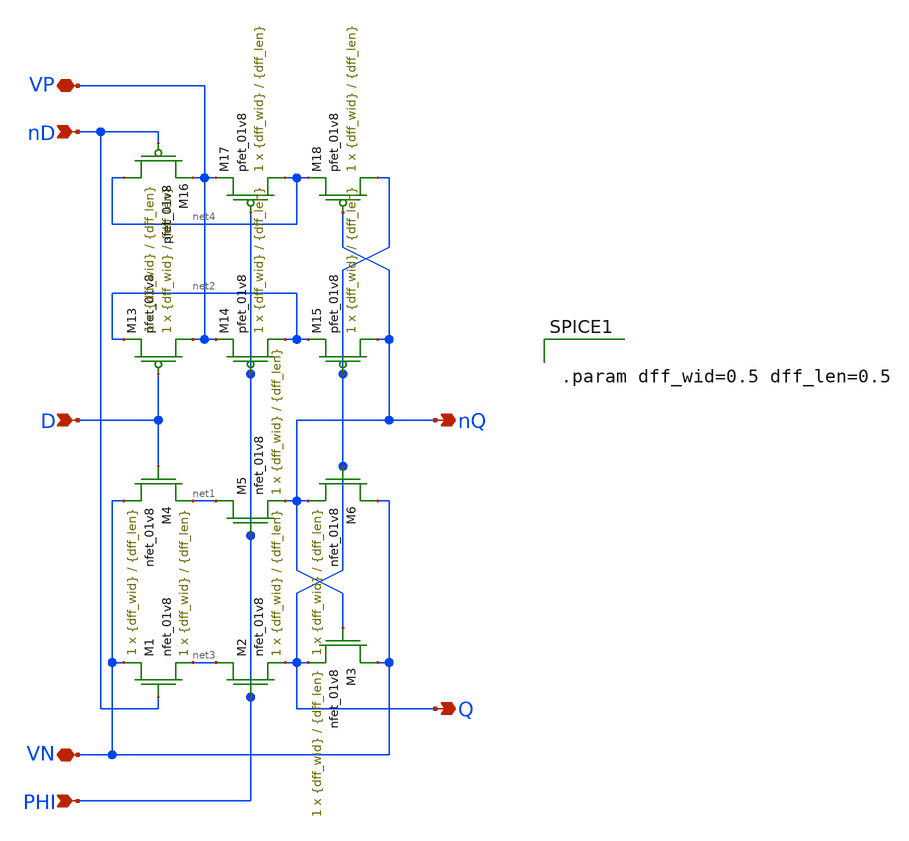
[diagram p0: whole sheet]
** sch_path: LDS/LDS_n_csrl_latch.sch
**.subckt LDS_n_csrl_latch D nD nQ Q PHI VP VN
*.ipin D
*.ipin nD
*.opin nQ
*.opin Q
*.ipin PHI
*.iopin VP
*.iopin VN
XM1 VN nD net3 VN sky130_fd_pr__nfet_01v8 L={dff_len} W={dff_wid} nf=1 ad='int((nf+1)/2) * W/nf * 0.29'
+ as='int((nf+2)/2) * W/nf * 0.29' pd='2*int((nf+1)/2) * (W/nf + 0.29)' ps='2*int((nf+2)/2) * (W/nf + 0.29)'
+ nrd='0.29 / W' nrs='0.29 / W' sa=0 sb=0 sd=0 mult=1 m=1
XM2 net3 PHI Q VN sky130_fd_pr__nfet_01v8 L={dff_len} W={dff_wid} nf=1 ad='int((nf+1)/2) * W/nf * 0.29'
+ as='int((nf+2)/2) * W/nf * 0.29' pd='2*int((nf+1)/2) * (W/nf + 0.29)' ps='2*int((nf+2)/2) * (W/nf + 0.29)'
+ nrd='0.29 / W' nrs='0.29 / W' sa=0 sb=0 sd=0 mult=1 m=1
XM3 VN nQ Q VN sky130_fd_pr__nfet_01v8 L={dff_len} W={dff_wid} nf=1 ad='int((nf+1)/2) * W/nf * 0.29'
+ as='int((nf+2)/2) * W/nf * 0.29' pd='2*int((nf+1)/2) * (W/nf + 0.29)' ps='2*int((nf+2)/2) * (W/nf + 0.29)'
+ nrd='0.29 / W' nrs='0.29 / W' sa=0 sb=0 sd=0 mult=1 m=1
XM4 net1 D VN VN sky130_fd_pr__nfet_01v8 L={dff_len} W={dff_wid} nf=1 ad='int((nf+1)/2) * W/nf * 0.29'
+ as='int((nf+2)/2) * W/nf * 0.29' pd='2*int((nf+1)/2) * (W/nf + 0.29)' ps='2*int((nf+2)/2) * (W/nf + 0.29)'
+ nrd='0.29 / W' nrs='0.29 / W' sa=0 sb=0 sd=0 mult=1 m=1
XM5 net1 PHI nQ VN sky130_fd_pr__nfet_01v8 L={dff_len} W={dff_wid} nf=1 ad='int((nf+1)/2) * W/nf * 0.29'
+ as='int((nf+2)/2) * W/nf * 0.29' pd='2*int((nf+1)/2) * (W/nf + 0.29)' ps='2*int((nf+2)/2) * (W/nf + 0.29)'
+ nrd='0.29 / W' nrs='0.29 / W' sa=0 sb=0 sd=0 mult=1 m=1
XM6 VN Q nQ VN sky130_fd_pr__nfet_01v8 L={dff_len} W={dff_wid} nf=1 ad='int((nf+1)/2) * W/nf * 0.29'
+ as='int((nf+2)/2) * W/nf * 0.29' pd='2*int((nf+1)/2) * (W/nf + 0.29)' ps='2*int((nf+2)/2) * (W/nf + 0.29)'
+ nrd='0.29 / W' nrs='0.29 / W' sa=0 sb=0 sd=0 mult=1 m=1
XM13 VP D net2 VP sky130_fd_pr__pfet_01v8 L={dff_len} W={dff_wid} nf=1 ad='int((nf+1)/2) * W/nf * 0.29'
+ as='int((nf+2)/2) * W/nf * 0.29' pd='2*int((nf+1)/2) * (W/nf + 0.29)' ps='2*int((nf+2)/2) * (W/nf + 0.29)'
+ nrd='0.29 / W' nrs='0.29 / W' sa=0 sb=0 sd=0 mult=1 m=1
XM14 net2 PHI VP VP sky130_fd_pr__pfet_01v8 L={dff_len} W={dff_wid} nf=1 ad='int((nf+1)/2) * W/nf * 0.29'
+ as='int((nf+2)/2) * W/nf * 0.29' pd='2*int((nf+1)/2) * (W/nf + 0.29)' ps='2*int((nf+2)/2) * (W/nf + 0.29)'
+ nrd='0.29 / W' nrs='0.29 / W' sa=0 sb=0 sd=0 mult=1 m=1
XM15 nQ Q net2 VP sky130_fd_pr__pfet_01v8 L={dff_len} W={dff_wid} nf=1 ad='int((nf+1)/2) * W/nf * 0.29'
+ as='int((nf+2)/2) * W/nf * 0.29' pd='2*int((nf+1)/2) * (W/nf + 0.29)' ps='2*int((nf+2)/2) * (W/nf + 0.29)'
+ nrd='0.29 / W' nrs='0.29 / W' sa=0 sb=0 sd=0 mult=1 m=1
XM16 net4 nD VP VP sky130_fd_pr__pfet_01v8 L={dff_len} W={dff_wid} nf=1 ad='int((nf+1)/2) * W/nf * 0.29'
+ as='int((nf+2)/2) * W/nf * 0.29' pd='2*int((nf+1)/2) * (W/nf + 0.29)' ps='2*int((nf+2)/2) * (W/nf + 0.29)'
+ nrd='0.29 / W' nrs='0.29 / W' sa=0 sb=0 sd=0 mult=1 m=1
XM17 net4 PHI VP VP sky130_fd_pr__pfet_01v8 L={dff_len} W={dff_wid} nf=1 ad='int((nf+1)/2) * W/nf * 0.29'
+ as='int((nf+2)/2) * W/nf * 0.29' pd='2*int((nf+1)/2) * (W/nf + 0.29)' ps='2*int((nf+2)/2) * (W/nf + 0.29)'
+ nrd='0.29 / W' nrs='0.29 / W' sa=0 sb=0 sd=0 mult=1 m=1
XM18 Q nQ net4 VP sky130_fd_pr__pfet_01v8 L={dff_len} W={dff_wid} nf=1 ad='int((nf+1)/2) * W/nf * 0.29'
+ as='int((nf+2)/2) * W/nf * 0.29' pd='2*int((nf+1)/2) * (W/nf + 0.29)' ps='2*int((nf+2)/2) * (W/nf + 0.29)'
+ nrd='0.29 / W' nrs='0.29 / W' sa=0 sb=0 sd=0 mult=1 m=1
**** begin user architecture code


.param dff_wid=0.5 dff_len=0.5


**** end user architecture code
**.ends
.end
